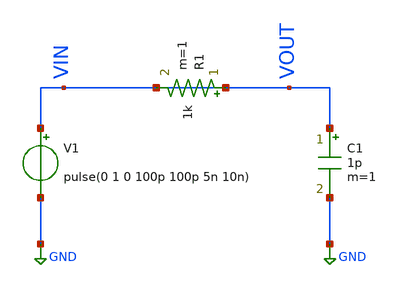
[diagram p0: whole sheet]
** sch_path: Designs/my_first_schematic.sch
**.subckt my_first_schematic
V1 VIN GND pulse(0 1 0 100p 100p 5n 10n)
C1 VOUT GND 1p m=1
R1 VOUT VIN 1k m=1
**** begin user architecture code


.tran 10p 50n
.save all


**** end user architecture code
**.ends
.GLOBAL GND
.end
